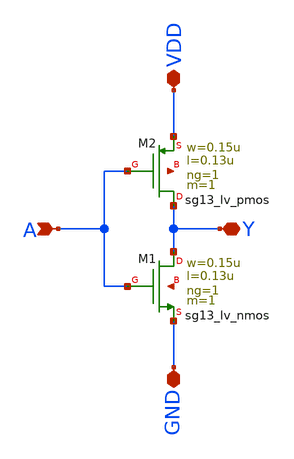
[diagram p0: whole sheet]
** sch_path: xschem/push_pull.sch
**.subckt push_pull A VDD Y GND
*.ipin A
*.iopin VDD
*.iopin Y
*.iopin GND
XM1 Y A GND net1 sg13_lv_nmos w=0.15u l=0.13u ng=1 m=1 mm_ok=1
XM2 Y A VDD net2 sg13_lv_pmos w=0.15u l=0.13u ng=1 m=1 mm_ok=1
**.ends
.end
